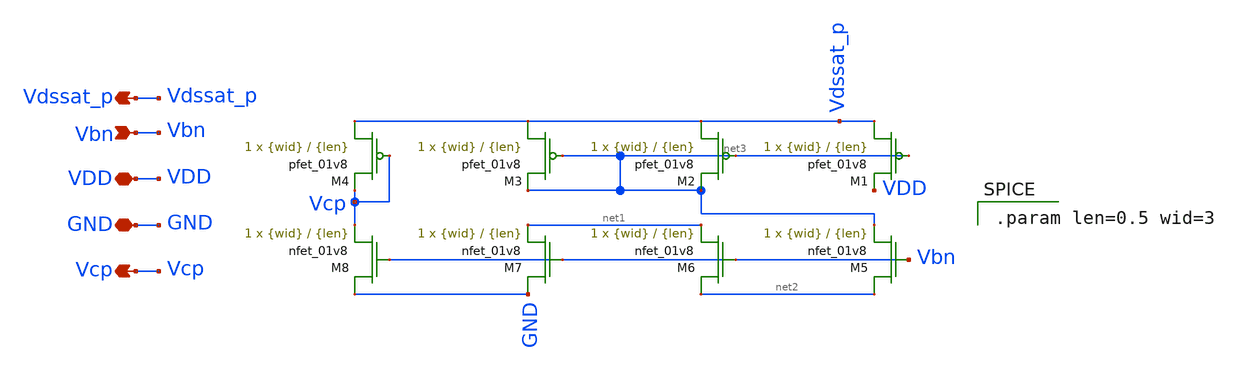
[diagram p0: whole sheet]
** sch_path: final/LDS/cascode_bias_pmos_LDS.sch
**.subckt cascode_bias_pmos_LDS Vbn VDD GND Vcp Vdssat_p
*.ipin Vbn
*.iopin VDD
*.iopin GND
*.opin Vcp
*.opin Vdssat_p
XM1 Vdssat_p net3 VDD VDD sky130_fd_pr__pfet_01v8 L={len} W={wid} nf=1 ad='int((nf+1)/2) * W/nf * 0.29'
+ as='int((nf+2)/2) * W/nf * 0.29' pd='2*int((nf+1)/2) * (W/nf + 0.29)' ps='2*int((nf+2)/2) * (W/nf + 0.29)'
+ nrd='0.29 / W' nrs='0.29 / W' sa=0 sb=0 sd=0 mult=1 m=1
XM2 Vdssat_p net3 net3 VDD sky130_fd_pr__pfet_01v8 L={len} W={wid} nf=1 ad='int((nf+1)/2) * W/nf * 0.29'
+ as='int((nf+2)/2) * W/nf * 0.29' pd='2*int((nf+1)/2) * (W/nf + 0.29)' ps='2*int((nf+2)/2) * (W/nf + 0.29)'
+ nrd='0.29 / W' nrs='0.29 / W' sa=0 sb=0 sd=0 mult=1 m=1
XM3 Vdssat_p net3 net3 VDD sky130_fd_pr__pfet_01v8 L={len} W={wid} nf=1 ad='int((nf+1)/2) * W/nf * 0.29'
+ as='int((nf+2)/2) * W/nf * 0.29' pd='2*int((nf+1)/2) * (W/nf + 0.29)' ps='2*int((nf+2)/2) * (W/nf + 0.29)'
+ nrd='0.29 / W' nrs='0.29 / W' sa=0 sb=0 sd=0 mult=1 m=1
XM4 Vdssat_p Vcp Vcp VDD sky130_fd_pr__pfet_01v8 L={len} W={wid} nf=1 ad='int((nf+1)/2) * W/nf * 0.29'
+ as='int((nf+2)/2) * W/nf * 0.29' pd='2*int((nf+1)/2) * (W/nf + 0.29)' ps='2*int((nf+2)/2) * (W/nf + 0.29)'
+ nrd='0.29 / W' nrs='0.29 / W' sa=0 sb=0 sd=0 mult=1 m=1
XM5 net2 Vbn net3 GND sky130_fd_pr__nfet_01v8 L={len} W={wid} nf=1 ad='int((nf+1)/2) * W/nf * 0.29' as='int((nf+2)/2) * W/nf * 0.29'
+ pd='2*int((nf+1)/2) * (W/nf + 0.29)' ps='2*int((nf+2)/2) * (W/nf + 0.29)' nrd='0.29 / W' nrs='0.29 / W'
+ sa=0 sb=0 sd=0 mult=1 m=1
XM6 net2 Vbn net1 GND sky130_fd_pr__nfet_01v8 L={len} W={wid} nf=1 ad='int((nf+1)/2) * W/nf * 0.29' as='int((nf+2)/2) * W/nf * 0.29'
+ pd='2*int((nf+1)/2) * (W/nf + 0.29)' ps='2*int((nf+2)/2) * (W/nf + 0.29)' nrd='0.29 / W' nrs='0.29 / W'
+ sa=0 sb=0 sd=0 mult=1 m=1
XM7 GND Vbn net1 GND sky130_fd_pr__nfet_01v8 L={len} W={wid} nf=1 ad='int((nf+1)/2) * W/nf * 0.29' as='int((nf+2)/2) * W/nf * 0.29'
+ pd='2*int((nf+1)/2) * (W/nf + 0.29)' ps='2*int((nf+2)/2) * (W/nf + 0.29)' nrd='0.29 / W' nrs='0.29 / W'
+ sa=0 sb=0 sd=0 mult=1 m=1
XM8 GND Vbn Vcp GND sky130_fd_pr__nfet_01v8 L={len} W={wid} nf=1 ad='int((nf+1)/2) * W/nf * 0.29' as='int((nf+2)/2) * W/nf * 0.29'
+ pd='2*int((nf+1)/2) * (W/nf + 0.29)' ps='2*int((nf+2)/2) * (W/nf + 0.29)' nrd='0.29 / W' nrs='0.29 / W'
+ sa=0 sb=0 sd=0 mult=1 m=1
**** begin user architecture code

.param len=0.5 wid=3

**** end user architecture code
**.ends
.end
